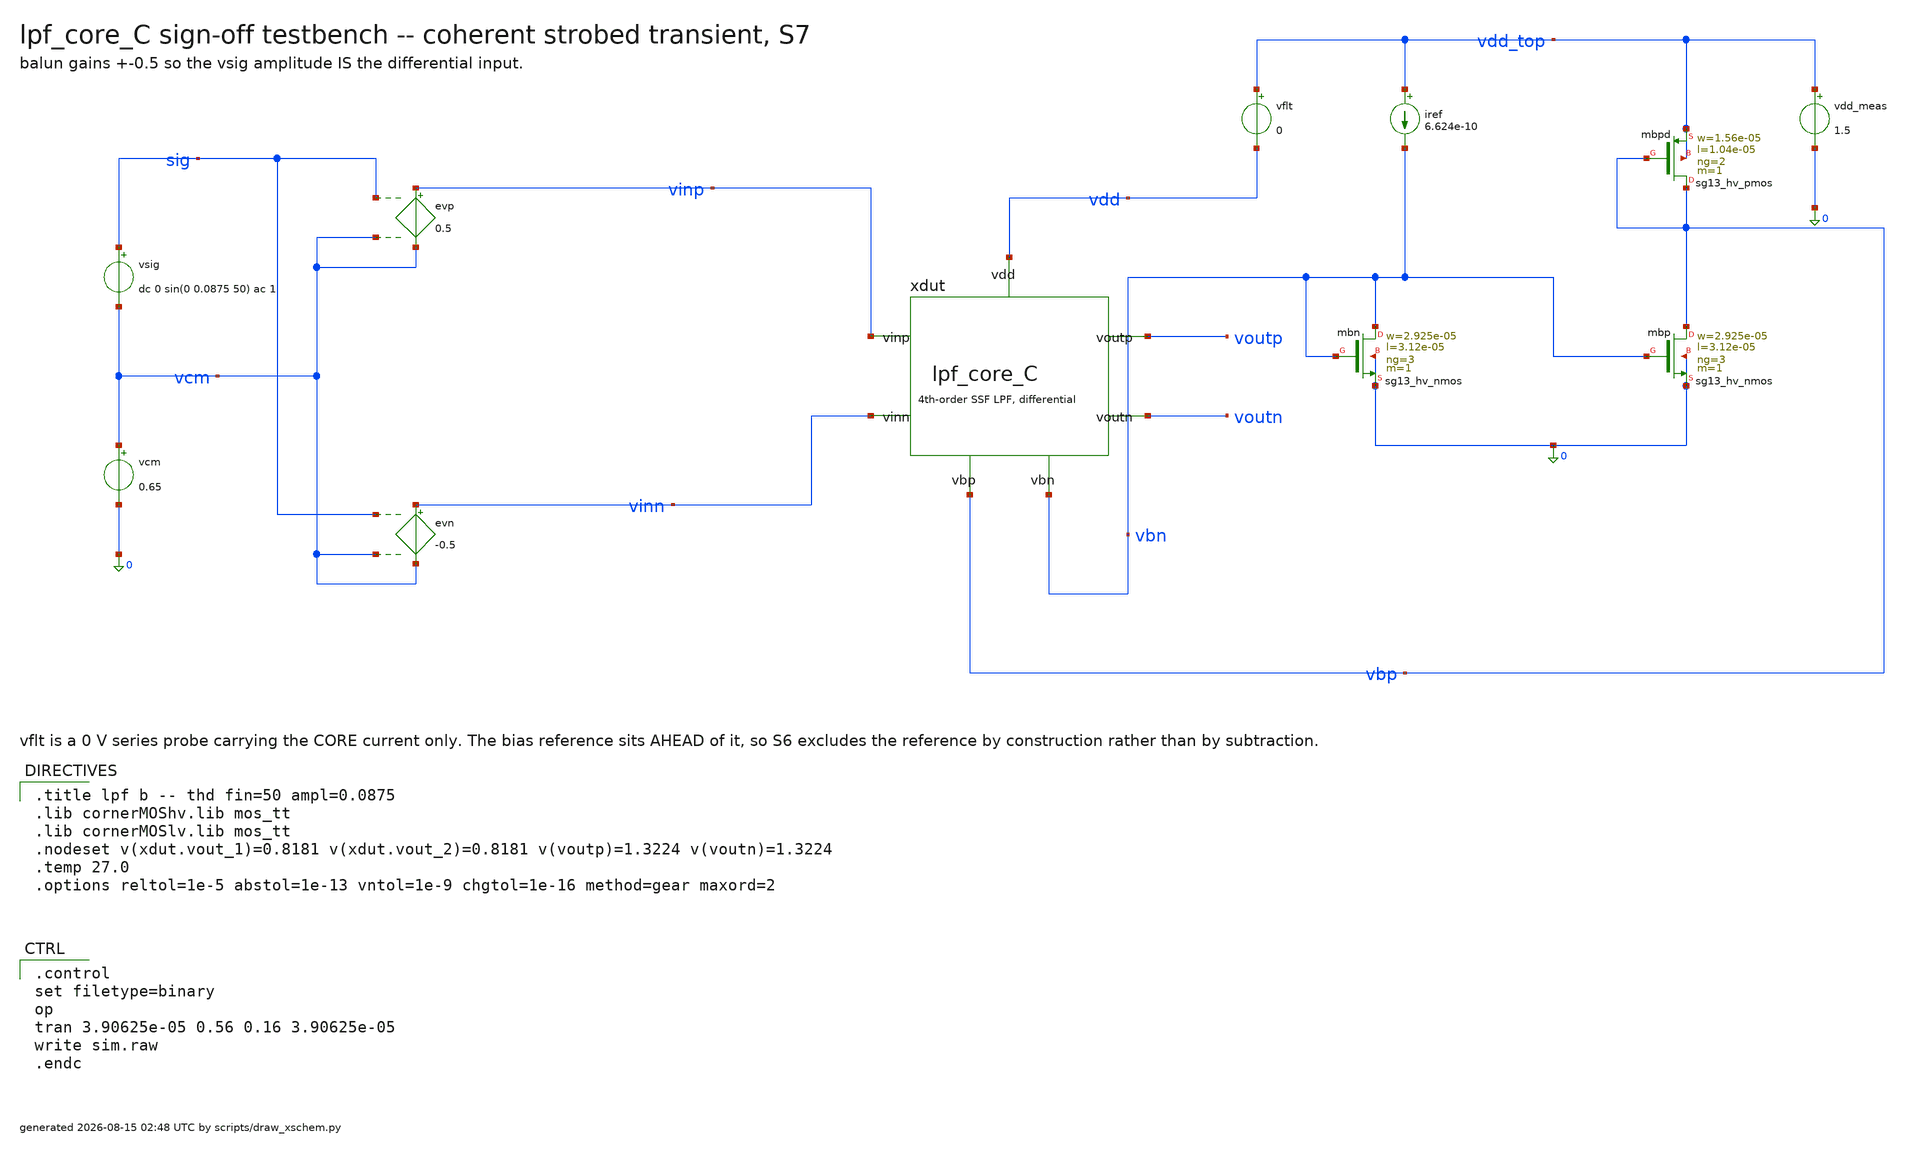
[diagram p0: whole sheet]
** sch_path: signoff/pre-pvt/C-lownoise/lpf_tb_C_thd.sch
**.subckt lpf_tb_C_thd
vsig sig vcm dc 0 sin(0 0.0875 50) ac 1
vcm vcm 0 0.65
evp vinp vcm sig vcm 0.5
evn vinn vcm sig vcm -0.5
xdut vinp vinn voutp voutn vbn vbp vdd lpf_core_C
vflt vdd_top vdd 0
vdd_meas vdd_top 0 1.5
iref vdd_top vbn 6.624e-10
Xmbn vbn vbn 0 0 sg13_hv_nmos w=2.925e-05 l=3.12e-05 ng=3 m=1 mm_ok=1
Xmbp vbp vbn 0 0 sg13_hv_nmos w=2.925e-05 l=3.12e-05 ng=3 m=1 mm_ok=1
Xmbpd vbp vbp vdd_top vdd_top sg13_hv_pmos w=1.56e-05 l=1.04e-05 ng=2 m=1 mm_ok=1
**** begin user architecture code

.title lpf b -- thd fin=50 ampl=0.0875
.lib cornerMOShv.lib mos_tt
.lib cornerMOSlv.lib mos_tt
.nodeset v(xdut.vout_1)=0.8181 v(xdut.vout_2)=0.8181 v(voutp)=1.3224 v(voutn)=1.3224
.temp 27.0
.options reltol=1e-5 abstol=1e-13 vntol=1e-9 chgtol=1e-16 method=gear maxord=2


.control
set filetype=binary
op
tran 3.90625e-05 0.56 0.16 3.90625e-05
write sim.raw
.endc

**** end user architecture code
**.ends
.end
